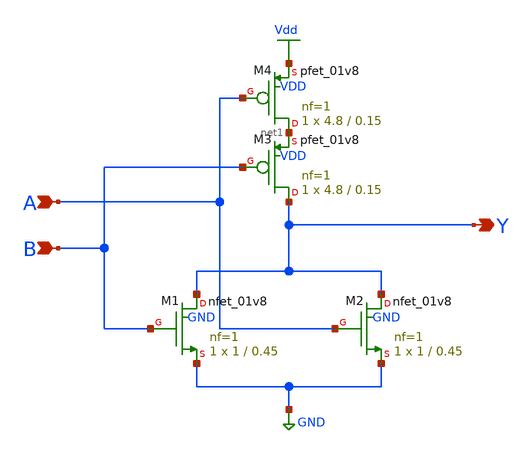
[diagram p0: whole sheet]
** sch_path: Circuiti/logic_gates_sch_sym/nor_2.sch
**.subckt nor_2 Y A B
*.opin Y
*.ipin A
*.ipin B
XM1 Y B GND GND sky130_fd_pr__nfet_01v8 L=0.45 W=1 nf=1 ad='int((nf+1)/2) * W/nf * 0.29' as='int((nf+2)/2) * W/nf * 0.29'
+ pd='2*int((nf+1)/2) * (W/nf + 0.29)' ps='2*int((nf+2)/2) * (W/nf + 0.29)' nrd='0.29 / W' nrs='0.29 / W'
+ sa=0 sb=0 sd=0 mult=1 m=1
XM3 Y B net1 VDD sky130_fd_pr__pfet_01v8 L=0.15 W=4.8 nf=1 ad='int((nf+1)/2) * W/nf * 0.29' as='int((nf+2)/2) * W/nf * 0.29'
+ pd='2*int((nf+1)/2) * (W/nf + 0.29)' ps='2*int((nf+2)/2) * (W/nf + 0.29)' nrd='0.29 / W' nrs='0.29 / W'
+ sa=0 sb=0 sd=0 mult=1 m=1
XM4 net1 A Vdd VDD sky130_fd_pr__pfet_01v8 L=0.15 W=4.8 nf=1 ad='int((nf+1)/2) * W/nf * 0.29' as='int((nf+2)/2) * W/nf * 0.29'
+ pd='2*int((nf+1)/2) * (W/nf + 0.29)' ps='2*int((nf+2)/2) * (W/nf + 0.29)' nrd='0.29 / W' nrs='0.29 / W'
+ sa=0 sb=0 sd=0 mult=1 m=1
XM2 Y A GND GND sky130_fd_pr__nfet_01v8 L=0.45 W=1 nf=1 ad='int((nf+1)/2) * W/nf * 0.29' as='int((nf+2)/2) * W/nf * 0.29'
+ pd='2*int((nf+1)/2) * (W/nf + 0.29)' ps='2*int((nf+2)/2) * (W/nf + 0.29)' nrd='0.29 / W' nrs='0.29 / W'
+ sa=0 sb=0 sd=0 mult=1 m=1
**.ends
.GLOBAL Vdd
.GLOBAL GND
.end
